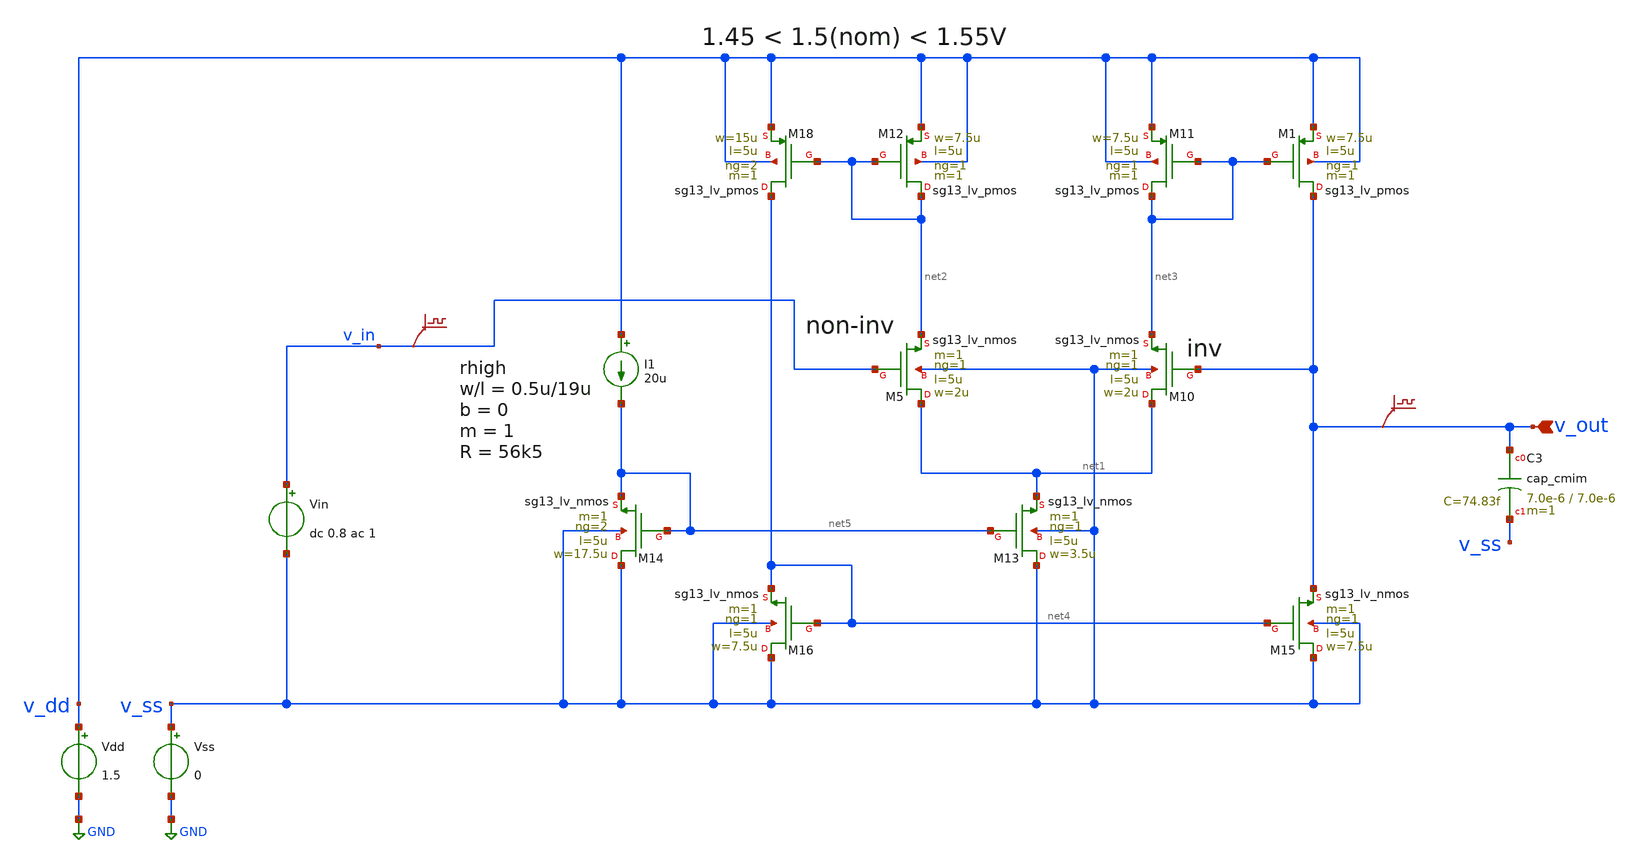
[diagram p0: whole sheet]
** sch_path: 3_Real_Cir/10_Real_Cir/test_Real_Cir/Improved/improved_5t_ota_v2_tb_A.sch
* Copyright 2023 IHP PDK Authors
* Licensed under the Apache License, Version 2.0 (the "License");
* you may not use this file except in compliance with the License.
* You may obtain a copy of the License at
* https://www.apache.org/licenses/LICENSE-2.0
* Unless required by applicable law or agreed to in writing, software
* distributed under the License is distributed on an "AS IS" BASIS,
* WITHOUT WARRANTIES OR CONDITIONS OF ANY KIND, either express or implied.
* See the License for the specific language governing permissions and
* limitations under the License.
* Copyright 2024 IHP PDK Authors
**.subckt improved_5t_ota_v2_tb_A v_out
*.ipin v_out
Vdd v_dd GND 1.5
Vss v_ss GND 0
Vin v_in v_ss dc 0.8 ac 1
.save v(v_in)
XM11 net3 net3 v_dd v_dd sg13_lv_pmos w=7.5u l=5u ng=1 m=1 mm_ok=1
XM12 net2 net2 v_dd v_dd sg13_lv_pmos w=7.5u l=5u ng=1 m=1 mm_ok=1
XM13 v_ss net5 net1 v_ss sg13_lv_nmos w=3.5u l=5u ng=1 m=1 mm_ok=1
XM16 v_ss net4 net4 v_ss sg13_lv_nmos w=7.5u l=5u ng=1 m=1 mm_ok=1
XM5 net1 v_in net2 v_ss sg13_lv_nmos w=2u l=5u ng=1 m=1 mm_ok=1
XM15 v_ss net4 v_out v_ss sg13_lv_nmos w=7.5u l=5u ng=1 m=1 mm_ok=1
XM18 net4 net2 v_dd v_dd sg13_lv_pmos w=15u l=5u ng=2 m=1 mm_ok=1
XM14 v_ss net5 net5 v_ss sg13_lv_nmos w=17.5u l=5u ng=2 m=1 mm_ok=1
XM10 net1 v_out net3 v_ss sg13_lv_nmos w=2u l=5u ng=1 m=1 mm_ok=1
.save v(v_out)
I1 v_dd net5 20u
XC3 v_out v_ss cap_cmim w=7.0e-6 l=7.0e-6 m=1 mm_ok=1
XM1 v_out net3 v_dd v_dd sg13_lv_pmos w=7.5u l=5u ng=1 m=1 mm_ok=1
**** begin user architecture code


.temp 27
.control
option sparse
save all
op
write ota-5t_tb-ac.raw
set appendwrite

ac dec 101 1k 100MEG
write ota-5t_tb-ac.raw

.title Mein Schwein pfeift

plot 20*log10(v_out) xlabel notimeforcaution ylabel atten(ua)tion/gain

meas ac dcgain MAX vmag(v_out) FROM=10 TO=10k
let f3db = dcgain/sqrt(2)
meas ac fbw WHEN vmag(v_out)=f3db FALL=1
let gainerror=(dcgain-1)/1
print dcgain
print fbw
print gainerror

noise v(v_out) Vin dec 101 1k 100MEG
print onoise_total

.endc


 .lib cornerMOSlv.lib mos_tt

 .lib $::SG13G2_MODELS/cornerMOSlv.lib mos_tt
.lib $::SG13G2_MODELS/cornerCAP.lib cap_typ
.inc $::PDK_ROOT/ihp-sg13g2/libs.ref/sg13g2_stdcell/spice/sg13g2_stdcell.spice

**** end user architecture code
**.ends
.GLOBAL GND
.end
